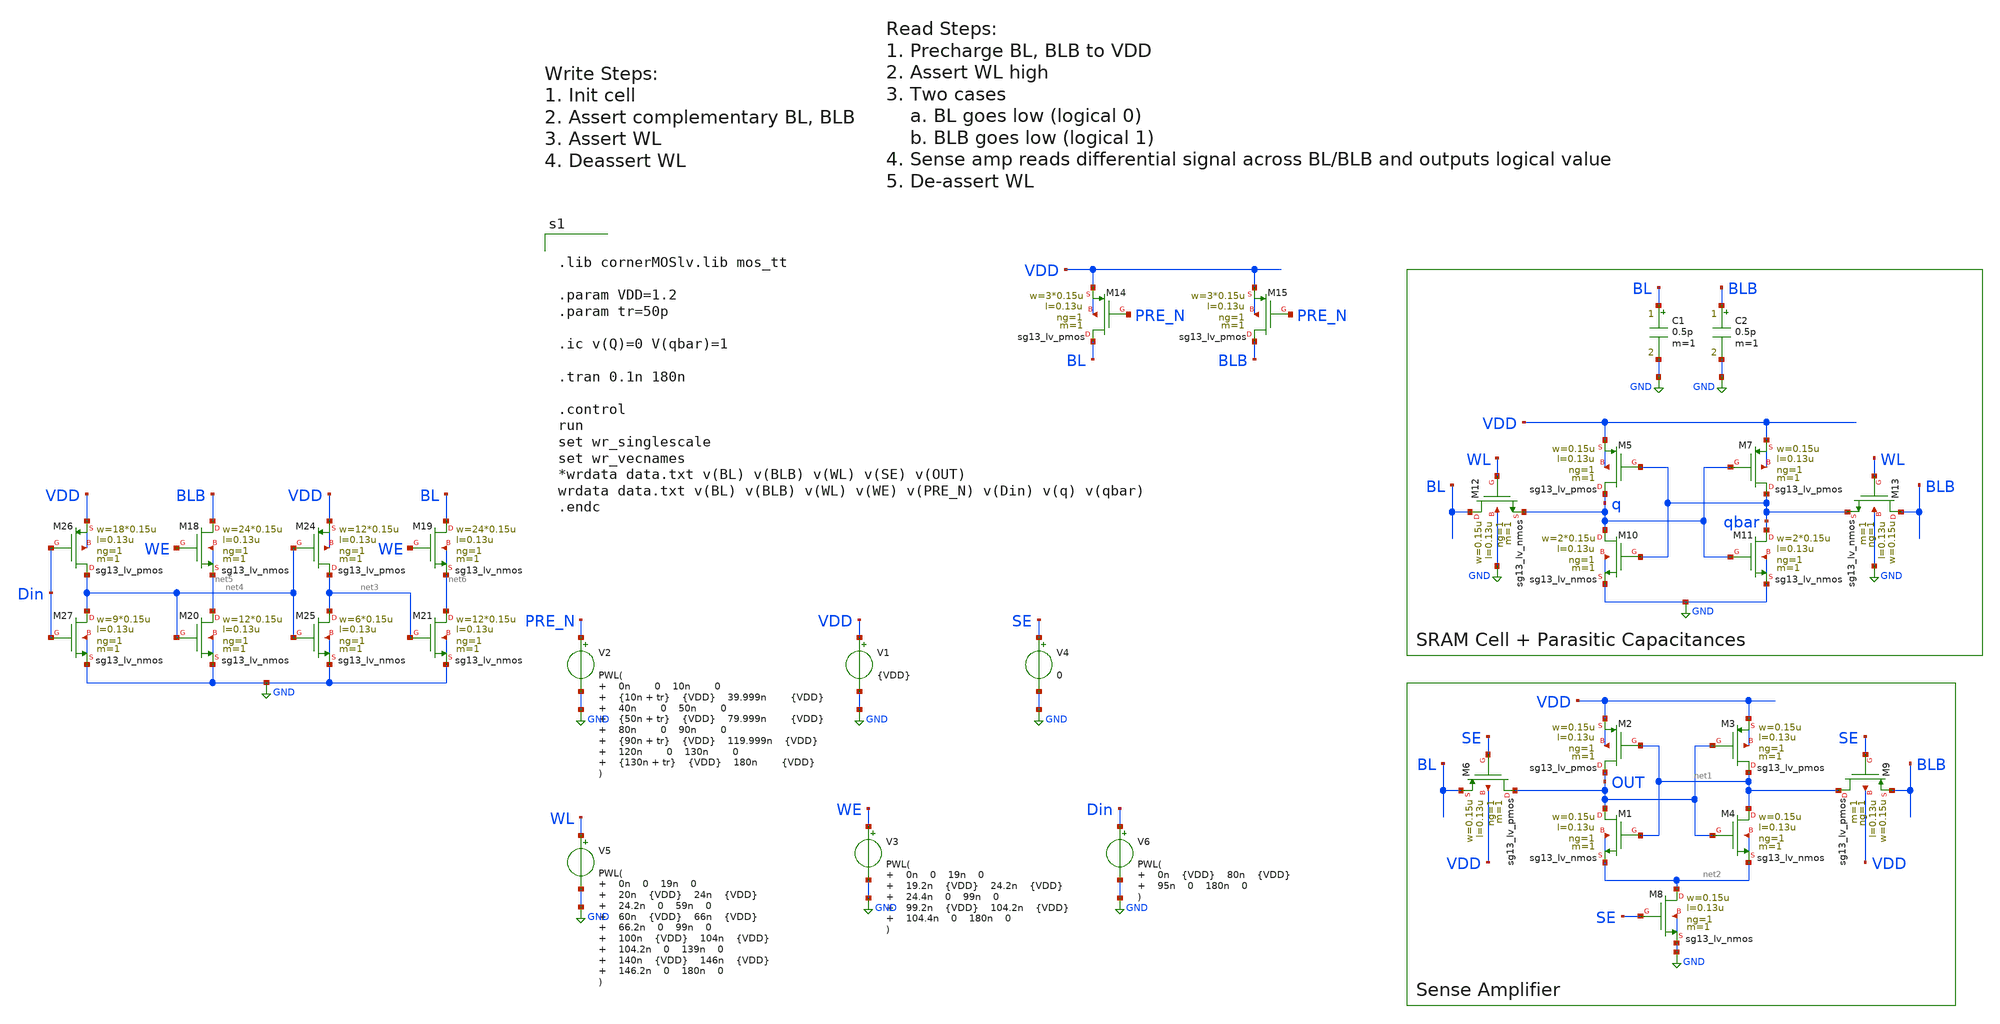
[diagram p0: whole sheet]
** sch_path: xschem/sram-sense-amp.sch
**.subckt sram-sense-amp
V1 VDD GND {VDD}
V4 SE GND 0
XM8 net2 SE GND GND sg13_lv_nmos w=0.15u l=0.13u ng=1 m=1 mm_ok=1
XM1 OUT net1 net2 net2 sg13_lv_nmos w=0.15u l=0.13u ng=1 m=1 mm_ok=1
XM3 net1 OUT VDD VDD sg13_lv_pmos w=0.15u l=0.13u ng=1 m=1 mm_ok=1
XM2 OUT net1 VDD VDD sg13_lv_pmos w=0.15u l=0.13u ng=1 m=1 mm_ok=1
XM4 net1 OUT net2 net2 sg13_lv_nmos w=0.15u l=0.13u ng=1 m=1 mm_ok=1
XM5 q qbar VDD VDD sg13_lv_pmos w=0.15u l=0.13u ng=1 m=1 mm_ok=1
XM7 qbar q VDD VDD sg13_lv_pmos w=0.15u l=0.13u ng=1 m=1 mm_ok=1
XM10 q qbar GND GND sg13_lv_nmos w=2*0.15u l=0.13u ng=1 m=1 mm_ok=1
XM11 qbar q GND GND sg13_lv_nmos w=2*0.15u l=0.13u ng=1 m=1 mm_ok=1
XM12 BL WL q GND sg13_lv_nmos w=0.15u l=0.13u ng=1 m=1 mm_ok=1
XM13 BLB WL qbar GND sg13_lv_nmos w=0.15u l=0.13u ng=1 m=1 mm_ok=1
C1 BL GND 0.5p m=1
C2 BLB GND 0.5p m=1
V5 WL GND PWL( 0n 0 19n 0 20n {VDD} 24n {VDD} 24.2n 0 59n 0 60n {VDD} 66n {VDD} 66.2n 0 99n 0 100n {VDD}
+ 104n {VDD} 104.2n 0 139n 0 140n {VDD} 146n {VDD} 146.2n 0 180n 0
)
XM6 OUT SE BL VDD sg13_lv_pmos w=0.15u l=0.13u ng=1 m=1 mm_ok=1
XM9 net1 SE BLB VDD sg13_lv_pmos w=0.15u l=0.13u ng=1 m=1 mm_ok=1
XM14 BL PRE_N VDD VDD sg13_lv_pmos w=3*0.15u l=0.13u ng=1 m=1 mm_ok=1
XM15 BLB PRE_N VDD VDD sg13_lv_pmos w=3*0.15u l=0.13u ng=1 m=1 mm_ok=1
V2 PRE_N GND PWL( 0n 0 10n 0 {10n + tr} {VDD} 39.999n {VDD} 40n 0 50n 0 {50n + tr} {VDD} 79.999n {VDD}
+ 80n 0 90n 0 {90n + tr} {VDD} 119.999n {VDD} 120n 0 130n 0 {130n + tr} {VDD} 180n {VDD}
)
XM18 BLB WE net5 net5 sg13_lv_nmos w=24*0.15u l=0.13u ng=1 m=1 mm_ok=1
XM19 BL WE net6 net6 sg13_lv_nmos w=24*0.15u l=0.13u ng=1 m=1 mm_ok=1
XM20 net5 net4 GND GND sg13_lv_nmos w=12*0.15u l=0.13u ng=1 m=1 mm_ok=1
XM21 net6 net3 GND GND sg13_lv_nmos w=12*0.15u l=0.13u ng=1 m=1 mm_ok=1
XM24 net3 net4 VDD VDD sg13_lv_pmos w=12*0.15u l=0.13u ng=1 m=1 mm_ok=1
XM25 net3 net4 GND GND sg13_lv_nmos w=6*0.15u l=0.13u ng=1 m=1 mm_ok=1
XM26 net4 Din VDD VDD sg13_lv_pmos w=18*0.15u l=0.13u ng=1 m=1 mm_ok=1
XM27 net4 Din GND GND sg13_lv_nmos w=9*0.15u l=0.13u ng=1 m=1 mm_ok=1
V3 WE GND PWL( 0n 0 19n 0 19.2n {VDD} 24.2n {VDD} 24.4n 0 99n 0 99.2n {VDD} 104.2n {VDD} 104.4n 0 180n
+ 0
)
V6 Din GND PWL( 0n {VDD} 80n {VDD} 95n 0 180n 0
)
**** begin user architecture code


.lib cornerMOSlv.lib mos_tt

.param VDD=1.2
.param tr=50p

.ic v(Q)=0 V(qbar)=1

.tran 0.1n 180n

.control
run
set wr_singlescale
set wr_vecnames
*wrdata data.txt v(BL) v(BLB) v(WL) v(SE) v(OUT)
wrdata data.txt v(BL) v(BLB) v(WL) v(WE) v(PRE_N) v(Din) v(q) v(qbar)
.endc


**** end user architecture code
**.ends
.GLOBAL GND
.end
